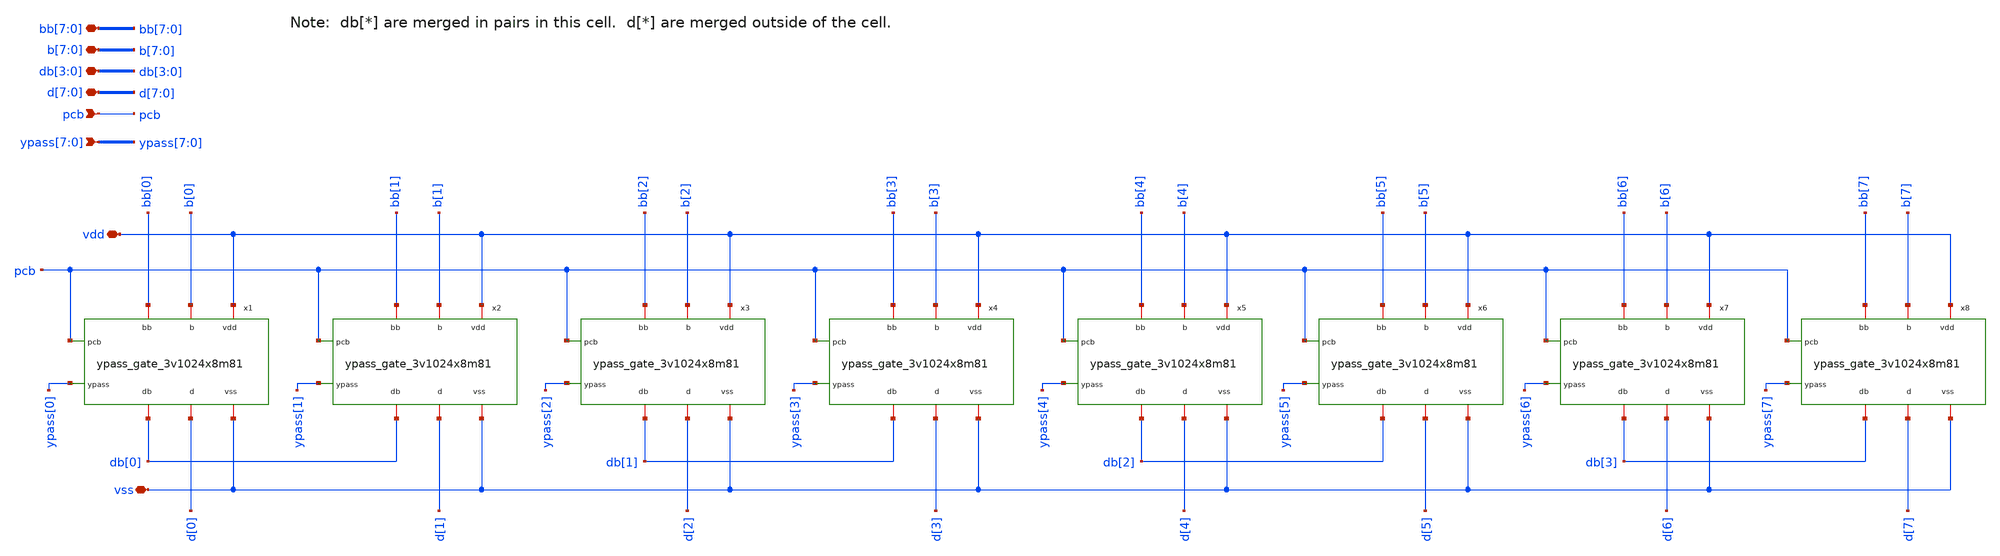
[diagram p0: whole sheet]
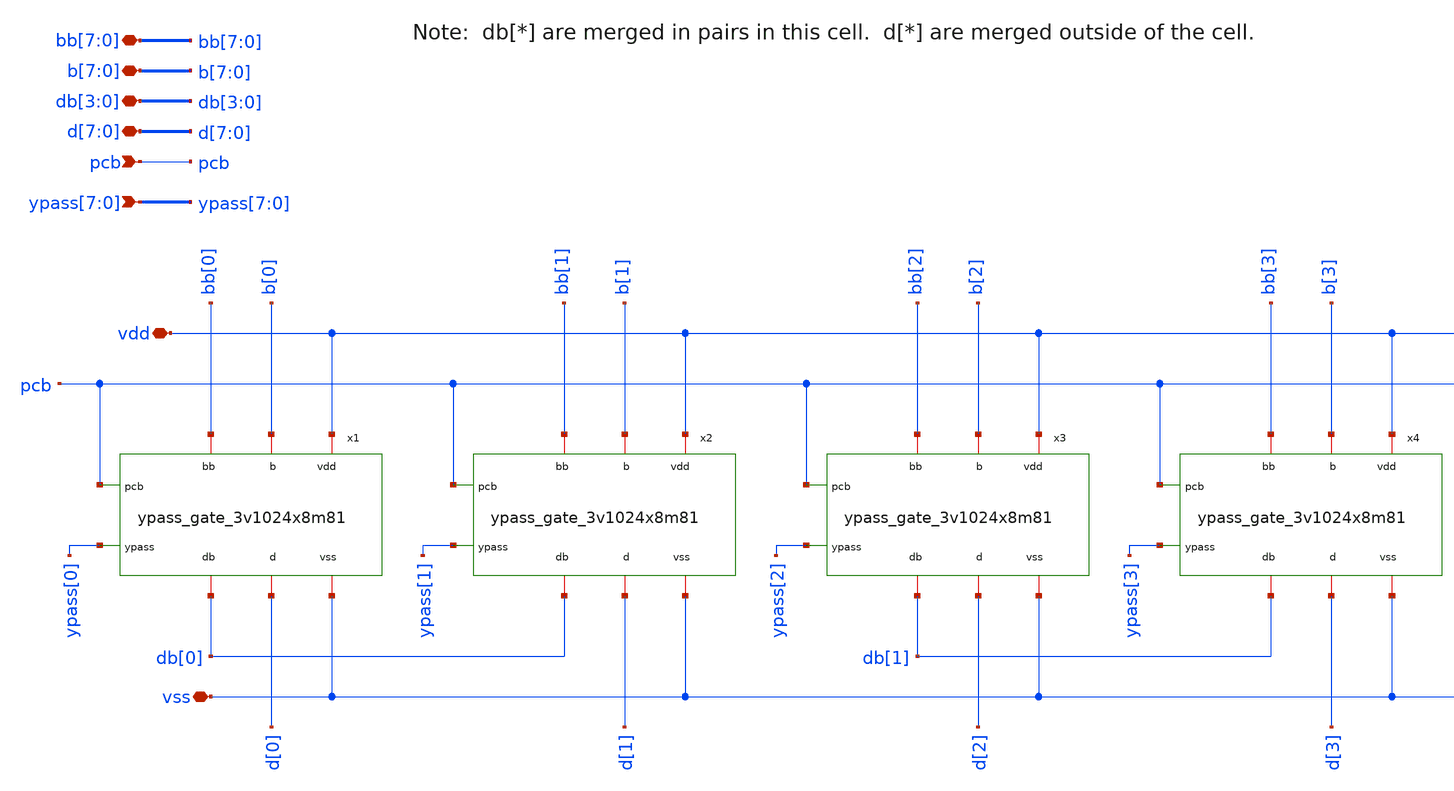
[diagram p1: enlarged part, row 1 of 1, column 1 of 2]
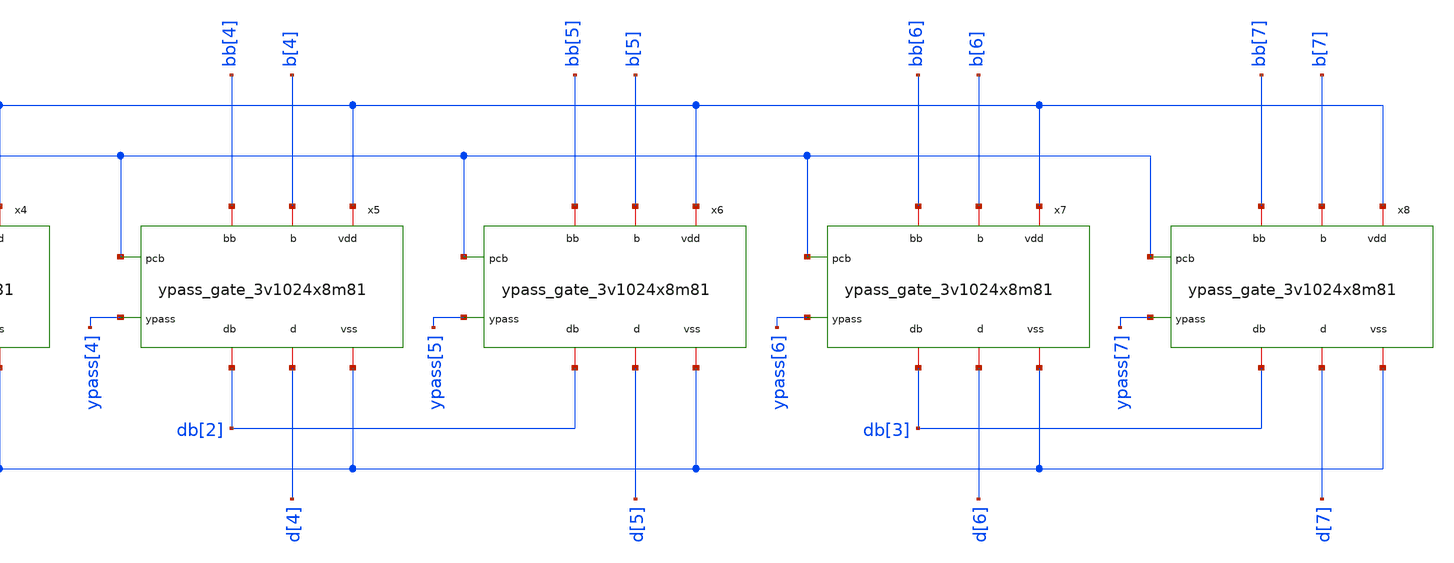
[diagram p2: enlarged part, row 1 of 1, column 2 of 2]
** sch_path: cells/gf180mcu_ocd_ip_sram__sram1024x8m8wm1/xschem/mux821_3v1024x8m81.sch
**.subckt mux821_3v1024x8m81 vdd vss bb[7],bb[6],bb[5],bb[4],bb[3],bb[2],bb[1],bb[0]
*+ b[7],b[6],b[5],b[4],b[3],b[2],b[1],b[0] db[3],db[2],db[1],db[0] pcb ypass[7],ypass[6],ypass[5],ypass[4],ypass[3],ypass[2],ypass[1],ypass[0]
*+ d[7],d[6],d[5],d[4],d[3],d[2],d[1],d[0]
*.iopin vdd
*.iopin vss
*.iopin bb[7],bb[6],bb[5],bb[4],bb[3],bb[2],bb[1],bb[0]
*.iopin b[7],b[6],b[5],b[4],b[3],b[2],b[1],b[0]
*.iopin db[3],db[2],db[1],db[0]
*.ipin pcb
*.ipin ypass[7],ypass[6],ypass[5],ypass[4],ypass[3],ypass[2],ypass[1],ypass[0]
*.iopin d[7],d[6],d[5],d[4],d[3],d[2],d[1],d[0]
x1 vdd ypass[0] pcb bb[0] b[0] db[0] d[0] vss ypass_gate_3v1024x8m81
x2 vdd ypass[1] pcb bb[1] b[1] db[0] d[1] vss ypass_gate_3v1024x8m81
x3 vdd ypass[2] pcb bb[2] b[2] db[1] d[2] vss ypass_gate_3v1024x8m81
x4 vdd ypass[3] pcb bb[3] b[3] db[1] d[3] vss ypass_gate_3v1024x8m81
x5 vdd ypass[4] pcb bb[4] b[4] db[2] d[4] vss ypass_gate_3v1024x8m81
x6 vdd ypass[5] pcb bb[5] b[5] db[2] d[5] vss ypass_gate_3v1024x8m81
x7 vdd ypass[6] pcb bb[6] b[6] db[3] d[6] vss ypass_gate_3v1024x8m81
x8 vdd ypass[7] pcb bb[7] b[7] db[3] d[7] vss ypass_gate_3v1024x8m81
**.ends
.end
